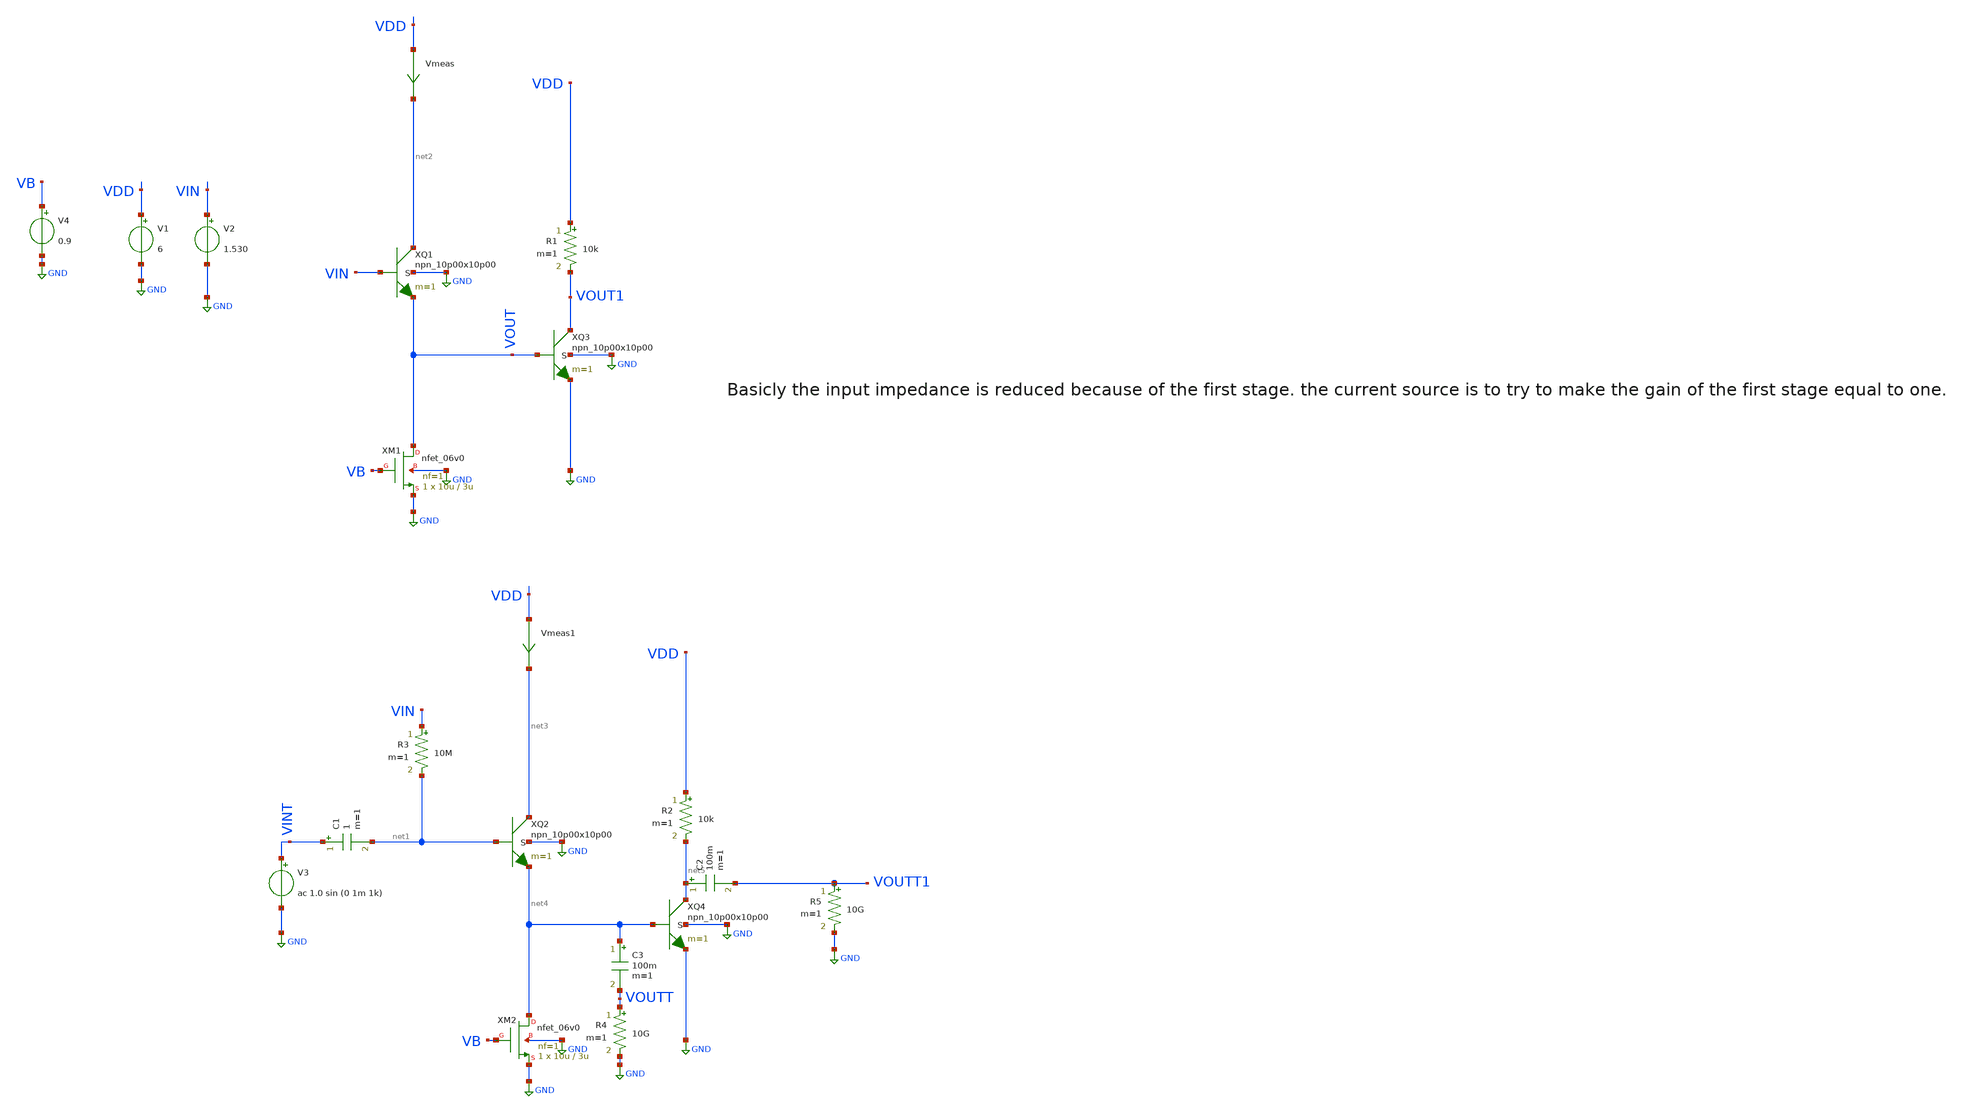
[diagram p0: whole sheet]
** sch_path: basic_circuits/bipolar_stage_cc_ce.sch
**.subckt bipolar_stage_cc_ce
Vmeas VDD net2 0
.save i(vmeas)
V1 VDD GND 6
V2 VIN GND 1.530
V3 VINT GND ac 1.0 sin (0 1m 1k)
R3 VIN net1 10M m=1
R5 VOUTT1 GND 10G m=1
V4 VB GND 0.9
C1 VINT net1 1 m=1
XQ1 net2 VIN VOUT GND npn_10p00x10p00 m=1
C2 net5 VOUTT1 100m m=1
XM1 VOUT VB GND GND nfet_06v0 L=3u W=10u nf=1 ad='int((nf+1)/2) * W/nf * 0.18u' as='int((nf+2)/2) * W/nf * 0.18u'
+ pd='2*int((nf+1)/2) * (W/nf + 0.18u)' ps='2*int((nf+2)/2) * (W/nf + 0.18u)' nrd='0.18u / W' nrs='0.18u / W'
+ sa=0 sb=0 sd=0 m=1
XQ3 VOUT1 VOUT GND GND npn_10p00x10p00 m=1
R1 VDD VOUT1 10k m=1
Vmeas1 VDD net3 0
.save i(vmeas1)
XQ2 net3 net1 net4 GND npn_10p00x10p00 m=1
XM2 net4 VB GND GND nfet_06v0 L=3u W=10u nf=1 ad='int((nf+1)/2) * W/nf * 0.18u' as='int((nf+2)/2) * W/nf * 0.18u'
+ pd='2*int((nf+1)/2) * (W/nf + 0.18u)' ps='2*int((nf+2)/2) * (W/nf + 0.18u)' nrd='0.18u / W' nrs='0.18u / W'
+ sa=0 sb=0 sd=0 m=1
XQ4 net5 net4 GND GND npn_10p00x10p00 m=1
R2 VDD net5 10k m=1
C3 net4 VOUTT 100m m=1
R4 VOUTT GND 10G m=1
**** begin user architecture code

**************************************************************
**************************************************************
**************************************************************
**************************************************************
**************************************************************
*LIBs*********************************************************
**************************************************************
**************************************************************
**************************************************************
**************************************************************
**************************************************************
.include $::180MCU_MODELS/design.ngspice
*.lib $::180MCU_MODELS/sm141064.ngspice statistical *use statistical if you want global and parameter mismatch
*.lib $::180MCU_MODELS/sm141064.ngspice res_statistical
.lib $::180MCU_MODELS/sm141064.ngspice typical
.lib $::180MCU_MODELS/sm141064.ngspice res_typical
.lib $::180MCU_MODELS/sm141064.ngspice moscap_typical
.lib $::180MCU_MODELS/sm141064.ngspice bjt_typical
.lib $::180MCU_MODELS/sm141064.ngspice diode_typical
.lib $::180MCU_MODELS/sm141064.ngspice mimcap_typical
**************************************************************
**************************************************************
**************************************************************
**************************************************************
**************************************************************
*Corners/montecarlo options***********************************
**************************************************************
**************************************************************
**************************************************************
**************************************************************
**************************************************************
.TEMP 27
.param   sw_stat_global = 1   sw_stat_mism = 1  mc_skew = 3  res_mc_skew = 3  cap_mc_skew = 3
+  fnoicor = 1
**************************************************************
**************************************************************
**************************************************************
**************************************************************
*SIMULATION and Plots*****************************************
**************************************************************
**************************************************************
**************************************************************
**************************************************************
.control
save all
dc V2 0 6 0.01
*dc simulation
plot v(VOUT) v(VIN) deriv(v(VOUT)) v(VOUT1)
plot v(VOUT1)  deriv(v(VOUT1))
*ploting VIN VOUT and the voltage gain
plot i(Vmeas)
*ploting the current for curiosity
tran 100ns 2m
*transient simulation
plot (v(VINT)) (v(VOUTT)) (v(VOUTT1))
*simple plot to exemplify the gain
fft v(VOUTT) v(VINT) (v(VOUTT1))
*fast fourier transfor
plot mag(v(VOUTT)) mag(v(VINT)) mag(v(VOUTT1))
* analyse the frequency spectrum of the transient waves, to detect distortion
ac dec 20 1 50G
*simple ac simulation
plot v(VOUTT1)
plot v(VOUTT)
*gain in function of the input frequency
.endc

**** end user architecture code
**.ends
.GLOBAL GND
.end
